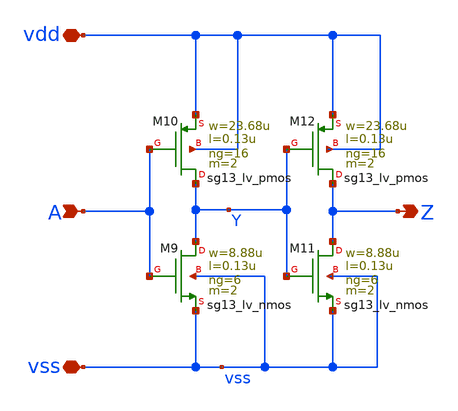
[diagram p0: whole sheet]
** sch_path: v2_feature_extr/untitled-1.sch
**.subckt untitled-1 A Z vdd vss
*.ipin A
*.opin Z
*.iopin vdd
*.iopin vss
XM9 Y A vss vss sg13_lv_nmos w=8.88u l=0.13u ng=6 m=2 mm_ok=1
XM10 Y A vdd vdd sg13_lv_pmos w=23.68u l=0.13u ng=16 m=2 mm_ok=1
XM11 Z Y vss vss sg13_lv_nmos w=8.88u l=0.13u ng=6 m=2 mm_ok=1
XM12 Z Y vdd vdd sg13_lv_pmos w=23.68u l=0.13u ng=16 m=2 mm_ok=1
**.ends
.end
